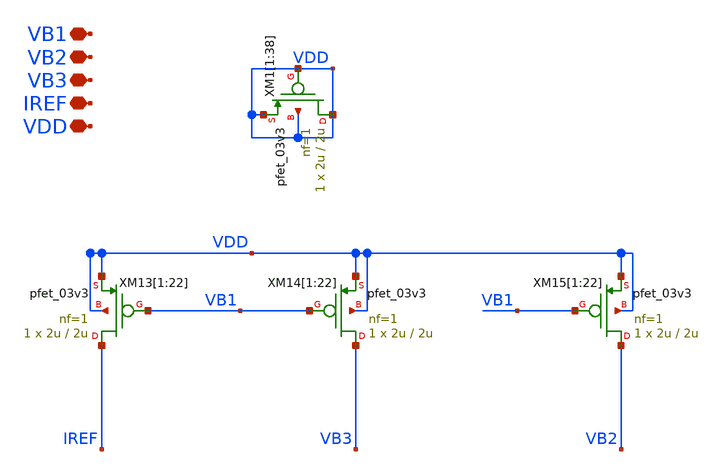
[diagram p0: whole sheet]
** sch_path: TIA_Filter/Folded/FC_bias_pfets.sch
**.subckt FC_bias_pfets IREF VDD VB1 VB2 VB3
*.iopin IREF
*.iopin VDD
*.iopin VB1
*.iopin VB2
*.iopin VB3
XM13[1] IREF VB1 VDD VDD pfet_03v3 L=2u W=2u nf=1 ad='int((nf+1)/2) * W/nf * 0.18u' as='int((nf+2)/2) * W/nf * 0.18u'
+ pd='2*int((nf+1)/2) * (W/nf + 0.18u)' ps='2*int((nf+2)/2) * (W/nf + 0.18u)' nrd='0.18u / W' nrs='0.18u / W'
+ sa=0 sb=0 sd=0 m=1
XM13[2] IREF VB1 VDD VDD pfet_03v3 L=2u W=2u nf=1 ad='int((nf+1)/2) * W/nf * 0.18u' as='int((nf+2)/2) * W/nf * 0.18u'
+ pd='2*int((nf+1)/2) * (W/nf + 0.18u)' ps='2*int((nf+2)/2) * (W/nf + 0.18u)' nrd='0.18u / W' nrs='0.18u / W'
+ sa=0 sb=0 sd=0 m=1
XM13[3] IREF VB1 VDD VDD pfet_03v3 L=2u W=2u nf=1 ad='int((nf+1)/2) * W/nf * 0.18u' as='int((nf+2)/2) * W/nf * 0.18u'
+ pd='2*int((nf+1)/2) * (W/nf + 0.18u)' ps='2*int((nf+2)/2) * (W/nf + 0.18u)' nrd='0.18u / W' nrs='0.18u / W'
+ sa=0 sb=0 sd=0 m=1
XM13[4] IREF VB1 VDD VDD pfet_03v3 L=2u W=2u nf=1 ad='int((nf+1)/2) * W/nf * 0.18u' as='int((nf+2)/2) * W/nf * 0.18u'
+ pd='2*int((nf+1)/2) * (W/nf + 0.18u)' ps='2*int((nf+2)/2) * (W/nf + 0.18u)' nrd='0.18u / W' nrs='0.18u / W'
+ sa=0 sb=0 sd=0 m=1
XM13[5] IREF VB1 VDD VDD pfet_03v3 L=2u W=2u nf=1 ad='int((nf+1)/2) * W/nf * 0.18u' as='int((nf+2)/2) * W/nf * 0.18u'
+ pd='2*int((nf+1)/2) * (W/nf + 0.18u)' ps='2*int((nf+2)/2) * (W/nf + 0.18u)' nrd='0.18u / W' nrs='0.18u / W'
+ sa=0 sb=0 sd=0 m=1
XM13[6] IREF VB1 VDD VDD pfet_03v3 L=2u W=2u nf=1 ad='int((nf+1)/2) * W/nf * 0.18u' as='int((nf+2)/2) * W/nf * 0.18u'
+ pd='2*int((nf+1)/2) * (W/nf + 0.18u)' ps='2*int((nf+2)/2) * (W/nf + 0.18u)' nrd='0.18u / W' nrs='0.18u / W'
+ sa=0 sb=0 sd=0 m=1
XM13[7] IREF VB1 VDD VDD pfet_03v3 L=2u W=2u nf=1 ad='int((nf+1)/2) * W/nf * 0.18u' as='int((nf+2)/2) * W/nf * 0.18u'
+ pd='2*int((nf+1)/2) * (W/nf + 0.18u)' ps='2*int((nf+2)/2) * (W/nf + 0.18u)' nrd='0.18u / W' nrs='0.18u / W'
+ sa=0 sb=0 sd=0 m=1
XM13[8] IREF VB1 VDD VDD pfet_03v3 L=2u W=2u nf=1 ad='int((nf+1)/2) * W/nf * 0.18u' as='int((nf+2)/2) * W/nf * 0.18u'
+ pd='2*int((nf+1)/2) * (W/nf + 0.18u)' ps='2*int((nf+2)/2) * (W/nf + 0.18u)' nrd='0.18u / W' nrs='0.18u / W'
+ sa=0 sb=0 sd=0 m=1
XM13[9] IREF VB1 VDD VDD pfet_03v3 L=2u W=2u nf=1 ad='int((nf+1)/2) * W/nf * 0.18u' as='int((nf+2)/2) * W/nf * 0.18u'
+ pd='2*int((nf+1)/2) * (W/nf + 0.18u)' ps='2*int((nf+2)/2) * (W/nf + 0.18u)' nrd='0.18u / W' nrs='0.18u / W'
+ sa=0 sb=0 sd=0 m=1
XM13[10] IREF VB1 VDD VDD pfet_03v3 L=2u W=2u nf=1 ad='int((nf+1)/2) * W/nf * 0.18u' as='int((nf+2)/2) * W/nf * 0.18u'
+ pd='2*int((nf+1)/2) * (W/nf + 0.18u)' ps='2*int((nf+2)/2) * (W/nf + 0.18u)' nrd='0.18u / W' nrs='0.18u / W'
+ sa=0 sb=0 sd=0 m=1
XM13[11] IREF VB1 VDD VDD pfet_03v3 L=2u W=2u nf=1 ad='int((nf+1)/2) * W/nf * 0.18u' as='int((nf+2)/2) * W/nf * 0.18u'
+ pd='2*int((nf+1)/2) * (W/nf + 0.18u)' ps='2*int((nf+2)/2) * (W/nf + 0.18u)' nrd='0.18u / W' nrs='0.18u / W'
+ sa=0 sb=0 sd=0 m=1
XM13[12] IREF VB1 VDD VDD pfet_03v3 L=2u W=2u nf=1 ad='int((nf+1)/2) * W/nf * 0.18u' as='int((nf+2)/2) * W/nf * 0.18u'
+ pd='2*int((nf+1)/2) * (W/nf + 0.18u)' ps='2*int((nf+2)/2) * (W/nf + 0.18u)' nrd='0.18u / W' nrs='0.18u / W'
+ sa=0 sb=0 sd=0 m=1
XM13[13] IREF VB1 VDD VDD pfet_03v3 L=2u W=2u nf=1 ad='int((nf+1)/2) * W/nf * 0.18u' as='int((nf+2)/2) * W/nf * 0.18u'
+ pd='2*int((nf+1)/2) * (W/nf + 0.18u)' ps='2*int((nf+2)/2) * (W/nf + 0.18u)' nrd='0.18u / W' nrs='0.18u / W'
+ sa=0 sb=0 sd=0 m=1
XM13[14] IREF VB1 VDD VDD pfet_03v3 L=2u W=2u nf=1 ad='int((nf+1)/2) * W/nf * 0.18u' as='int((nf+2)/2) * W/nf * 0.18u'
+ pd='2*int((nf+1)/2) * (W/nf + 0.18u)' ps='2*int((nf+2)/2) * (W/nf + 0.18u)' nrd='0.18u / W' nrs='0.18u / W'
+ sa=0 sb=0 sd=0 m=1
XM13[15] IREF VB1 VDD VDD pfet_03v3 L=2u W=2u nf=1 ad='int((nf+1)/2) * W/nf * 0.18u' as='int((nf+2)/2) * W/nf * 0.18u'
+ pd='2*int((nf+1)/2) * (W/nf + 0.18u)' ps='2*int((nf+2)/2) * (W/nf + 0.18u)' nrd='0.18u / W' nrs='0.18u / W'
+ sa=0 sb=0 sd=0 m=1
XM13[16] IREF VB1 VDD VDD pfet_03v3 L=2u W=2u nf=1 ad='int((nf+1)/2) * W/nf * 0.18u' as='int((nf+2)/2) * W/nf * 0.18u'
+ pd='2*int((nf+1)/2) * (W/nf + 0.18u)' ps='2*int((nf+2)/2) * (W/nf + 0.18u)' nrd='0.18u / W' nrs='0.18u / W'
+ sa=0 sb=0 sd=0 m=1
XM13[17] IREF VB1 VDD VDD pfet_03v3 L=2u W=2u nf=1 ad='int((nf+1)/2) * W/nf * 0.18u' as='int((nf+2)/2) * W/nf * 0.18u'
+ pd='2*int((nf+1)/2) * (W/nf + 0.18u)' ps='2*int((nf+2)/2) * (W/nf + 0.18u)' nrd='0.18u / W' nrs='0.18u / W'
+ sa=0 sb=0 sd=0 m=1
XM13[18] IREF VB1 VDD VDD pfet_03v3 L=2u W=2u nf=1 ad='int((nf+1)/2) * W/nf * 0.18u' as='int((nf+2)/2) * W/nf * 0.18u'
+ pd='2*int((nf+1)/2) * (W/nf + 0.18u)' ps='2*int((nf+2)/2) * (W/nf + 0.18u)' nrd='0.18u / W' nrs='0.18u / W'
+ sa=0 sb=0 sd=0 m=1
XM13[19] IREF VB1 VDD VDD pfet_03v3 L=2u W=2u nf=1 ad='int((nf+1)/2) * W/nf * 0.18u' as='int((nf+2)/2) * W/nf * 0.18u'
+ pd='2*int((nf+1)/2) * (W/nf + 0.18u)' ps='2*int((nf+2)/2) * (W/nf + 0.18u)' nrd='0.18u / W' nrs='0.18u / W'
+ sa=0 sb=0 sd=0 m=1
XM13[20] IREF VB1 VDD VDD pfet_03v3 L=2u W=2u nf=1 ad='int((nf+1)/2) * W/nf * 0.18u' as='int((nf+2)/2) * W/nf * 0.18u'
+ pd='2*int((nf+1)/2) * (W/nf + 0.18u)' ps='2*int((nf+2)/2) * (W/nf + 0.18u)' nrd='0.18u / W' nrs='0.18u / W'
+ sa=0 sb=0 sd=0 m=1
XM13[21] IREF VB1 VDD VDD pfet_03v3 L=2u W=2u nf=1 ad='int((nf+1)/2) * W/nf * 0.18u' as='int((nf+2)/2) * W/nf * 0.18u'
+ pd='2*int((nf+1)/2) * (W/nf + 0.18u)' ps='2*int((nf+2)/2) * (W/nf + 0.18u)' nrd='0.18u / W' nrs='0.18u / W'
+ sa=0 sb=0 sd=0 m=1
XM13[22] IREF VB1 VDD VDD pfet_03v3 L=2u W=2u nf=1 ad='int((nf+1)/2) * W/nf * 0.18u' as='int((nf+2)/2) * W/nf * 0.18u'
+ pd='2*int((nf+1)/2) * (W/nf + 0.18u)' ps='2*int((nf+2)/2) * (W/nf + 0.18u)' nrd='0.18u / W' nrs='0.18u / W'
+ sa=0 sb=0 sd=0 m=1
XM14[1] VB3 VB1 VDD VDD pfet_03v3 L=2u W=2u nf=1 ad='int((nf+1)/2) * W/nf * 0.18u' as='int((nf+2)/2) * W/nf * 0.18u'
+ pd='2*int((nf+1)/2) * (W/nf + 0.18u)' ps='2*int((nf+2)/2) * (W/nf + 0.18u)' nrd='0.18u / W' nrs='0.18u / W'
+ sa=0 sb=0 sd=0 m=1
XM14[2] VB3 VB1 VDD VDD pfet_03v3 L=2u W=2u nf=1 ad='int((nf+1)/2) * W/nf * 0.18u' as='int((nf+2)/2) * W/nf * 0.18u'
+ pd='2*int((nf+1)/2) * (W/nf + 0.18u)' ps='2*int((nf+2)/2) * (W/nf + 0.18u)' nrd='0.18u / W' nrs='0.18u / W'
+ sa=0 sb=0 sd=0 m=1
XM14[3] VB3 VB1 VDD VDD pfet_03v3 L=2u W=2u nf=1 ad='int((nf+1)/2) * W/nf * 0.18u' as='int((nf+2)/2) * W/nf * 0.18u'
+ pd='2*int((nf+1)/2) * (W/nf + 0.18u)' ps='2*int((nf+2)/2) * (W/nf + 0.18u)' nrd='0.18u / W' nrs='0.18u / W'
+ sa=0 sb=0 sd=0 m=1
XM14[4] VB3 VB1 VDD VDD pfet_03v3 L=2u W=2u nf=1 ad='int((nf+1)/2) * W/nf * 0.18u' as='int((nf+2)/2) * W/nf * 0.18u'
+ pd='2*int((nf+1)/2) * (W/nf + 0.18u)' ps='2*int((nf+2)/2) * (W/nf + 0.18u)' nrd='0.18u / W' nrs='0.18u / W'
+ sa=0 sb=0 sd=0 m=1
XM14[5] VB3 VB1 VDD VDD pfet_03v3 L=2u W=2u nf=1 ad='int((nf+1)/2) * W/nf * 0.18u' as='int((nf+2)/2) * W/nf * 0.18u'
+ pd='2*int((nf+1)/2) * (W/nf + 0.18u)' ps='2*int((nf+2)/2) * (W/nf + 0.18u)' nrd='0.18u / W' nrs='0.18u / W'
+ sa=0 sb=0 sd=0 m=1
XM14[6] VB3 VB1 VDD VDD pfet_03v3 L=2u W=2u nf=1 ad='int((nf+1)/2) * W/nf * 0.18u' as='int((nf+2)/2) * W/nf * 0.18u'
+ pd='2*int((nf+1)/2) * (W/nf + 0.18u)' ps='2*int((nf+2)/2) * (W/nf + 0.18u)' nrd='0.18u / W' nrs='0.18u / W'
+ sa=0 sb=0 sd=0 m=1
XM14[7] VB3 VB1 VDD VDD pfet_03v3 L=2u W=2u nf=1 ad='int((nf+1)/2) * W/nf * 0.18u' as='int((nf+2)/2) * W/nf * 0.18u'
+ pd='2*int((nf+1)/2) * (W/nf + 0.18u)' ps='2*int((nf+2)/2) * (W/nf + 0.18u)' nrd='0.18u / W' nrs='0.18u / W'
+ sa=0 sb=0 sd=0 m=1
XM14[8] VB3 VB1 VDD VDD pfet_03v3 L=2u W=2u nf=1 ad='int((nf+1)/2) * W/nf * 0.18u' as='int((nf+2)/2) * W/nf * 0.18u'
+ pd='2*int((nf+1)/2) * (W/nf + 0.18u)' ps='2*int((nf+2)/2) * (W/nf + 0.18u)' nrd='0.18u / W' nrs='0.18u / W'
+ sa=0 sb=0 sd=0 m=1
XM14[9] VB3 VB1 VDD VDD pfet_03v3 L=2u W=2u nf=1 ad='int((nf+1)/2) * W/nf * 0.18u' as='int((nf+2)/2) * W/nf * 0.18u'
+ pd='2*int((nf+1)/2) * (W/nf + 0.18u)' ps='2*int((nf+2)/2) * (W/nf + 0.18u)' nrd='0.18u / W' nrs='0.18u / W'
+ sa=0 sb=0 sd=0 m=1
XM14[10] VB3 VB1 VDD VDD pfet_03v3 L=2u W=2u nf=1 ad='int((nf+1)/2) * W/nf * 0.18u' as='int((nf+2)/2) * W/nf * 0.18u'
+ pd='2*int((nf+1)/2) * (W/nf + 0.18u)' ps='2*int((nf+2)/2) * (W/nf + 0.18u)' nrd='0.18u / W' nrs='0.18u / W'
+ sa=0 sb=0 sd=0 m=1
XM14[11] VB3 VB1 VDD VDD pfet_03v3 L=2u W=2u nf=1 ad='int((nf+1)/2) * W/nf * 0.18u' as='int((nf+2)/2) * W/nf * 0.18u'
+ pd='2*int((nf+1)/2) * (W/nf + 0.18u)' ps='2*int((nf+2)/2) * (W/nf + 0.18u)' nrd='0.18u / W' nrs='0.18u / W'
+ sa=0 sb=0 sd=0 m=1
XM14[12] VB3 VB1 VDD VDD pfet_03v3 L=2u W=2u nf=1 ad='int((nf+1)/2) * W/nf * 0.18u' as='int((nf+2)/2) * W/nf * 0.18u'
+ pd='2*int((nf+1)/2) * (W/nf + 0.18u)' ps='2*int((nf+2)/2) * (W/nf + 0.18u)' nrd='0.18u / W' nrs='0.18u / W'
+ sa=0 sb=0 sd=0 m=1
XM14[13] VB3 VB1 VDD VDD pfet_03v3 L=2u W=2u nf=1 ad='int((nf+1)/2) * W/nf * 0.18u' as='int((nf+2)/2) * W/nf * 0.18u'
+ pd='2*int((nf+1)/2) * (W/nf + 0.18u)' ps='2*int((nf+2)/2) * (W/nf + 0.18u)' nrd='0.18u / W' nrs='0.18u / W'
+ sa=0 sb=0 sd=0 m=1
XM14[14] VB3 VB1 VDD VDD pfet_03v3 L=2u W=2u nf=1 ad='int((nf+1)/2) * W/nf * 0.18u' as='int((nf+2)/2) * W/nf * 0.18u'
+ pd='2*int((nf+1)/2) * (W/nf + 0.18u)' ps='2*int((nf+2)/2) * (W/nf + 0.18u)' nrd='0.18u / W' nrs='0.18u / W'
+ sa=0 sb=0 sd=0 m=1
XM14[15] VB3 VB1 VDD VDD pfet_03v3 L=2u W=2u nf=1 ad='int((nf+1)/2) * W/nf * 0.18u' as='int((nf+2)/2) * W/nf * 0.18u'
+ pd='2*int((nf+1)/2) * (W/nf + 0.18u)' ps='2*int((nf+2)/2) * (W/nf + 0.18u)' nrd='0.18u / W' nrs='0.18u / W'
+ sa=0 sb=0 sd=0 m=1
XM14[16] VB3 VB1 VDD VDD pfet_03v3 L=2u W=2u nf=1 ad='int((nf+1)/2) * W/nf * 0.18u' as='int((nf+2)/2) * W/nf * 0.18u'
+ pd='2*int((nf+1)/2) * (W/nf + 0.18u)' ps='2*int((nf+2)/2) * (W/nf + 0.18u)' nrd='0.18u / W' nrs='0.18u / W'
+ sa=0 sb=0 sd=0 m=1
XM14[17] VB3 VB1 VDD VDD pfet_03v3 L=2u W=2u nf=1 ad='int((nf+1)/2) * W/nf * 0.18u' as='int((nf+2)/2) * W/nf * 0.18u'
+ pd='2*int((nf+1)/2) * (W/nf + 0.18u)' ps='2*int((nf+2)/2) * (W/nf + 0.18u)' nrd='0.18u / W' nrs='0.18u / W'
+ sa=0 sb=0 sd=0 m=1
XM14[18] VB3 VB1 VDD VDD pfet_03v3 L=2u W=2u nf=1 ad='int((nf+1)/2) * W/nf * 0.18u' as='int((nf+2)/2) * W/nf * 0.18u'
+ pd='2*int((nf+1)/2) * (W/nf + 0.18u)' ps='2*int((nf+2)/2) * (W/nf + 0.18u)' nrd='0.18u / W' nrs='0.18u / W'
+ sa=0 sb=0 sd=0 m=1
XM14[19] VB3 VB1 VDD VDD pfet_03v3 L=2u W=2u nf=1 ad='int((nf+1)/2) * W/nf * 0.18u' as='int((nf+2)/2) * W/nf * 0.18u'
+ pd='2*int((nf+1)/2) * (W/nf + 0.18u)' ps='2*int((nf+2)/2) * (W/nf + 0.18u)' nrd='0.18u / W' nrs='0.18u / W'
+ sa=0 sb=0 sd=0 m=1
XM14[20] VB3 VB1 VDD VDD pfet_03v3 L=2u W=2u nf=1 ad='int((nf+1)/2) * W/nf * 0.18u' as='int((nf+2)/2) * W/nf * 0.18u'
+ pd='2*int((nf+1)/2) * (W/nf + 0.18u)' ps='2*int((nf+2)/2) * (W/nf + 0.18u)' nrd='0.18u / W' nrs='0.18u / W'
+ sa=0 sb=0 sd=0 m=1
XM14[21] VB3 VB1 VDD VDD pfet_03v3 L=2u W=2u nf=1 ad='int((nf+1)/2) * W/nf * 0.18u' as='int((nf+2)/2) * W/nf * 0.18u'
+ pd='2*int((nf+1)/2) * (W/nf + 0.18u)' ps='2*int((nf+2)/2) * (W/nf + 0.18u)' nrd='0.18u / W' nrs='0.18u / W'
+ sa=0 sb=0 sd=0 m=1
XM14[22] VB3 VB1 VDD VDD pfet_03v3 L=2u W=2u nf=1 ad='int((nf+1)/2) * W/nf * 0.18u' as='int((nf+2)/2) * W/nf * 0.18u'
+ pd='2*int((nf+1)/2) * (W/nf + 0.18u)' ps='2*int((nf+2)/2) * (W/nf + 0.18u)' nrd='0.18u / W' nrs='0.18u / W'
+ sa=0 sb=0 sd=0 m=1
XM15[1] VB2 VB1 VDD VDD pfet_03v3 L=2u W=2u nf=1 ad='int((nf+1)/2) * W/nf * 0.18u' as='int((nf+2)/2) * W/nf * 0.18u'
+ pd='2*int((nf+1)/2) * (W/nf + 0.18u)' ps='2*int((nf+2)/2) * (W/nf + 0.18u)' nrd='0.18u / W' nrs='0.18u / W'
+ sa=0 sb=0 sd=0 m=1
XM15[2] VB2 VB1 VDD VDD pfet_03v3 L=2u W=2u nf=1 ad='int((nf+1)/2) * W/nf * 0.18u' as='int((nf+2)/2) * W/nf * 0.18u'
+ pd='2*int((nf+1)/2) * (W/nf + 0.18u)' ps='2*int((nf+2)/2) * (W/nf + 0.18u)' nrd='0.18u / W' nrs='0.18u / W'
+ sa=0 sb=0 sd=0 m=1
XM15[3] VB2 VB1 VDD VDD pfet_03v3 L=2u W=2u nf=1 ad='int((nf+1)/2) * W/nf * 0.18u' as='int((nf+2)/2) * W/nf * 0.18u'
+ pd='2*int((nf+1)/2) * (W/nf + 0.18u)' ps='2*int((nf+2)/2) * (W/nf + 0.18u)' nrd='0.18u / W' nrs='0.18u / W'
+ sa=0 sb=0 sd=0 m=1
XM15[4] VB2 VB1 VDD VDD pfet_03v3 L=2u W=2u nf=1 ad='int((nf+1)/2) * W/nf * 0.18u' as='int((nf+2)/2) * W/nf * 0.18u'
+ pd='2*int((nf+1)/2) * (W/nf + 0.18u)' ps='2*int((nf+2)/2) * (W/nf + 0.18u)' nrd='0.18u / W' nrs='0.18u / W'
+ sa=0 sb=0 sd=0 m=1
XM15[5] VB2 VB1 VDD VDD pfet_03v3 L=2u W=2u nf=1 ad='int((nf+1)/2) * W/nf * 0.18u' as='int((nf+2)/2) * W/nf * 0.18u'
+ pd='2*int((nf+1)/2) * (W/nf + 0.18u)' ps='2*int((nf+2)/2) * (W/nf + 0.18u)' nrd='0.18u / W' nrs='0.18u / W'
+ sa=0 sb=0 sd=0 m=1
XM15[6] VB2 VB1 VDD VDD pfet_03v3 L=2u W=2u nf=1 ad='int((nf+1)/2) * W/nf * 0.18u' as='int((nf+2)/2) * W/nf * 0.18u'
+ pd='2*int((nf+1)/2) * (W/nf + 0.18u)' ps='2*int((nf+2)/2) * (W/nf + 0.18u)' nrd='0.18u / W' nrs='0.18u / W'
+ sa=0 sb=0 sd=0 m=1
XM15[7] VB2 VB1 VDD VDD pfet_03v3 L=2u W=2u nf=1 ad='int((nf+1)/2) * W/nf * 0.18u' as='int((nf+2)/2) * W/nf * 0.18u'
+ pd='2*int((nf+1)/2) * (W/nf + 0.18u)' ps='2*int((nf+2)/2) * (W/nf + 0.18u)' nrd='0.18u / W' nrs='0.18u / W'
+ sa=0 sb=0 sd=0 m=1
XM15[8] VB2 VB1 VDD VDD pfet_03v3 L=2u W=2u nf=1 ad='int((nf+1)/2) * W/nf * 0.18u' as='int((nf+2)/2) * W/nf * 0.18u'
+ pd='2*int((nf+1)/2) * (W/nf + 0.18u)' ps='2*int((nf+2)/2) * (W/nf + 0.18u)' nrd='0.18u / W' nrs='0.18u / W'
+ sa=0 sb=0 sd=0 m=1
XM15[9] VB2 VB1 VDD VDD pfet_03v3 L=2u W=2u nf=1 ad='int((nf+1)/2) * W/nf * 0.18u' as='int((nf+2)/2) * W/nf * 0.18u'
+ pd='2*int((nf+1)/2) * (W/nf + 0.18u)' ps='2*int((nf+2)/2) * (W/nf + 0.18u)' nrd='0.18u / W' nrs='0.18u / W'
+ sa=0 sb=0 sd=0 m=1
XM15[10] VB2 VB1 VDD VDD pfet_03v3 L=2u W=2u nf=1 ad='int((nf+1)/2) * W/nf * 0.18u' as='int((nf+2)/2) * W/nf * 0.18u'
+ pd='2*int((nf+1)/2) * (W/nf + 0.18u)' ps='2*int((nf+2)/2) * (W/nf + 0.18u)' nrd='0.18u / W' nrs='0.18u / W'
+ sa=0 sb=0 sd=0 m=1
XM15[11] VB2 VB1 VDD VDD pfet_03v3 L=2u W=2u nf=1 ad='int((nf+1)/2) * W/nf * 0.18u' as='int((nf+2)/2) * W/nf * 0.18u'
+ pd='2*int((nf+1)/2) * (W/nf + 0.18u)' ps='2*int((nf+2)/2) * (W/nf + 0.18u)' nrd='0.18u / W' nrs='0.18u / W'
+ sa=0 sb=0 sd=0 m=1
XM15[12] VB2 VB1 VDD VDD pfet_03v3 L=2u W=2u nf=1 ad='int((nf+1)/2) * W/nf * 0.18u' as='int((nf+2)/2) * W/nf * 0.18u'
+ pd='2*int((nf+1)/2) * (W/nf + 0.18u)' ps='2*int((nf+2)/2) * (W/nf + 0.18u)' nrd='0.18u / W' nrs='0.18u / W'
+ sa=0 sb=0 sd=0 m=1
XM15[13] VB2 VB1 VDD VDD pfet_03v3 L=2u W=2u nf=1 ad='int((nf+1)/2) * W/nf * 0.18u' as='int((nf+2)/2) * W/nf * 0.18u'
+ pd='2*int((nf+1)/2) * (W/nf + 0.18u)' ps='2*int((nf+2)/2) * (W/nf + 0.18u)' nrd='0.18u / W' nrs='0.18u / W'
+ sa=0 sb=0 sd=0 m=1
XM15[14] VB2 VB1 VDD VDD pfet_03v3 L=2u W=2u nf=1 ad='int((nf+1)/2) * W/nf * 0.18u' as='int((nf+2)/2) * W/nf * 0.18u'
+ pd='2*int((nf+1)/2) * (W/nf + 0.18u)' ps='2*int((nf+2)/2) * (W/nf + 0.18u)' nrd='0.18u / W' nrs='0.18u / W'
+ sa=0 sb=0 sd=0 m=1
XM15[15] VB2 VB1 VDD VDD pfet_03v3 L=2u W=2u nf=1 ad='int((nf+1)/2) * W/nf * 0.18u' as='int((nf+2)/2) * W/nf * 0.18u'
+ pd='2*int((nf+1)/2) * (W/nf + 0.18u)' ps='2*int((nf+2)/2) * (W/nf + 0.18u)' nrd='0.18u / W' nrs='0.18u / W'
+ sa=0 sb=0 sd=0 m=1
XM15[16] VB2 VB1 VDD VDD pfet_03v3 L=2u W=2u nf=1 ad='int((nf+1)/2) * W/nf * 0.18u' as='int((nf+2)/2) * W/nf * 0.18u'
+ pd='2*int((nf+1)/2) * (W/nf + 0.18u)' ps='2*int((nf+2)/2) * (W/nf + 0.18u)' nrd='0.18u / W' nrs='0.18u / W'
+ sa=0 sb=0 sd=0 m=1
XM15[17] VB2 VB1 VDD VDD pfet_03v3 L=2u W=2u nf=1 ad='int((nf+1)/2) * W/nf * 0.18u' as='int((nf+2)/2) * W/nf * 0.18u'
+ pd='2*int((nf+1)/2) * (W/nf + 0.18u)' ps='2*int((nf+2)/2) * (W/nf + 0.18u)' nrd='0.18u / W' nrs='0.18u / W'
+ sa=0 sb=0 sd=0 m=1
XM15[18] VB2 VB1 VDD VDD pfet_03v3 L=2u W=2u nf=1 ad='int((nf+1)/2) * W/nf * 0.18u' as='int((nf+2)/2) * W/nf * 0.18u'
+ pd='2*int((nf+1)/2) * (W/nf + 0.18u)' ps='2*int((nf+2)/2) * (W/nf + 0.18u)' nrd='0.18u / W' nrs='0.18u / W'
+ sa=0 sb=0 sd=0 m=1
XM15[19] VB2 VB1 VDD VDD pfet_03v3 L=2u W=2u nf=1 ad='int((nf+1)/2) * W/nf * 0.18u' as='int((nf+2)/2) * W/nf * 0.18u'
+ pd='2*int((nf+1)/2) * (W/nf + 0.18u)' ps='2*int((nf+2)/2) * (W/nf + 0.18u)' nrd='0.18u / W' nrs='0.18u / W'
+ sa=0 sb=0 sd=0 m=1
XM15[20] VB2 VB1 VDD VDD pfet_03v3 L=2u W=2u nf=1 ad='int((nf+1)/2) * W/nf * 0.18u' as='int((nf+2)/2) * W/nf * 0.18u'
+ pd='2*int((nf+1)/2) * (W/nf + 0.18u)' ps='2*int((nf+2)/2) * (W/nf + 0.18u)' nrd='0.18u / W' nrs='0.18u / W'
+ sa=0 sb=0 sd=0 m=1
XM15[21] VB2 VB1 VDD VDD pfet_03v3 L=2u W=2u nf=1 ad='int((nf+1)/2) * W/nf * 0.18u' as='int((nf+2)/2) * W/nf * 0.18u'
+ pd='2*int((nf+1)/2) * (W/nf + 0.18u)' ps='2*int((nf+2)/2) * (W/nf + 0.18u)' nrd='0.18u / W' nrs='0.18u / W'
+ sa=0 sb=0 sd=0 m=1
XM15[22] VB2 VB1 VDD VDD pfet_03v3 L=2u W=2u nf=1 ad='int((nf+1)/2) * W/nf * 0.18u' as='int((nf+2)/2) * W/nf * 0.18u'
+ pd='2*int((nf+1)/2) * (W/nf + 0.18u)' ps='2*int((nf+2)/2) * (W/nf + 0.18u)' nrd='0.18u / W' nrs='0.18u / W'
+ sa=0 sb=0 sd=0 m=1
XM1[1] VDD VDD VDD VDD pfet_03v3 L=2u W=2u nf=1 ad='int((nf+1)/2) * W/nf * 0.18u' as='int((nf+2)/2) * W/nf * 0.18u'
+ pd='2*int((nf+1)/2) * (W/nf + 0.18u)' ps='2*int((nf+2)/2) * (W/nf + 0.18u)' nrd='0.18u / W' nrs='0.18u / W'
+ sa=0 sb=0 sd=0 m=1
XM1[2] VDD VDD VDD VDD pfet_03v3 L=2u W=2u nf=1 ad='int((nf+1)/2) * W/nf * 0.18u' as='int((nf+2)/2) * W/nf * 0.18u'
+ pd='2*int((nf+1)/2) * (W/nf + 0.18u)' ps='2*int((nf+2)/2) * (W/nf + 0.18u)' nrd='0.18u / W' nrs='0.18u / W'
+ sa=0 sb=0 sd=0 m=1
XM1[3] VDD VDD VDD VDD pfet_03v3 L=2u W=2u nf=1 ad='int((nf+1)/2) * W/nf * 0.18u' as='int((nf+2)/2) * W/nf * 0.18u'
+ pd='2*int((nf+1)/2) * (W/nf + 0.18u)' ps='2*int((nf+2)/2) * (W/nf + 0.18u)' nrd='0.18u / W' nrs='0.18u / W'
+ sa=0 sb=0 sd=0 m=1
XM1[4] VDD VDD VDD VDD pfet_03v3 L=2u W=2u nf=1 ad='int((nf+1)/2) * W/nf * 0.18u' as='int((nf+2)/2) * W/nf * 0.18u'
+ pd='2*int((nf+1)/2) * (W/nf + 0.18u)' ps='2*int((nf+2)/2) * (W/nf + 0.18u)' nrd='0.18u / W' nrs='0.18u / W'
+ sa=0 sb=0 sd=0 m=1
XM1[5] VDD VDD VDD VDD pfet_03v3 L=2u W=2u nf=1 ad='int((nf+1)/2) * W/nf * 0.18u' as='int((nf+2)/2) * W/nf * 0.18u'
+ pd='2*int((nf+1)/2) * (W/nf + 0.18u)' ps='2*int((nf+2)/2) * (W/nf + 0.18u)' nrd='0.18u / W' nrs='0.18u / W'
+ sa=0 sb=0 sd=0 m=1
XM1[6] VDD VDD VDD VDD pfet_03v3 L=2u W=2u nf=1 ad='int((nf+1)/2) * W/nf * 0.18u' as='int((nf+2)/2) * W/nf * 0.18u'
+ pd='2*int((nf+1)/2) * (W/nf + 0.18u)' ps='2*int((nf+2)/2) * (W/nf + 0.18u)' nrd='0.18u / W' nrs='0.18u / W'
+ sa=0 sb=0 sd=0 m=1
XM1[7] VDD VDD VDD VDD pfet_03v3 L=2u W=2u nf=1 ad='int((nf+1)/2) * W/nf * 0.18u' as='int((nf+2)/2) * W/nf * 0.18u'
+ pd='2*int((nf+1)/2) * (W/nf + 0.18u)' ps='2*int((nf+2)/2) * (W/nf + 0.18u)' nrd='0.18u / W' nrs='0.18u / W'
+ sa=0 sb=0 sd=0 m=1
XM1[8] VDD VDD VDD VDD pfet_03v3 L=2u W=2u nf=1 ad='int((nf+1)/2) * W/nf * 0.18u' as='int((nf+2)/2) * W/nf * 0.18u'
+ pd='2*int((nf+1)/2) * (W/nf + 0.18u)' ps='2*int((nf+2)/2) * (W/nf + 0.18u)' nrd='0.18u / W' nrs='0.18u / W'
+ sa=0 sb=0 sd=0 m=1
XM1[9] VDD VDD VDD VDD pfet_03v3 L=2u W=2u nf=1 ad='int((nf+1)/2) * W/nf * 0.18u' as='int((nf+2)/2) * W/nf * 0.18u'
+ pd='2*int((nf+1)/2) * (W/nf + 0.18u)' ps='2*int((nf+2)/2) * (W/nf + 0.18u)' nrd='0.18u / W' nrs='0.18u / W'
+ sa=0 sb=0 sd=0 m=1
XM1[10] VDD VDD VDD VDD pfet_03v3 L=2u W=2u nf=1 ad='int((nf+1)/2) * W/nf * 0.18u' as='int((nf+2)/2) * W/nf * 0.18u'
+ pd='2*int((nf+1)/2) * (W/nf + 0.18u)' ps='2*int((nf+2)/2) * (W/nf + 0.18u)' nrd='0.18u / W' nrs='0.18u / W'
+ sa=0 sb=0 sd=0 m=1
XM1[11] VDD VDD VDD VDD pfet_03v3 L=2u W=2u nf=1 ad='int((nf+1)/2) * W/nf * 0.18u' as='int((nf+2)/2) * W/nf * 0.18u'
+ pd='2*int((nf+1)/2) * (W/nf + 0.18u)' ps='2*int((nf+2)/2) * (W/nf + 0.18u)' nrd='0.18u / W' nrs='0.18u / W'
+ sa=0 sb=0 sd=0 m=1
XM1[12] VDD VDD VDD VDD pfet_03v3 L=2u W=2u nf=1 ad='int((nf+1)/2) * W/nf * 0.18u' as='int((nf+2)/2) * W/nf * 0.18u'
+ pd='2*int((nf+1)/2) * (W/nf + 0.18u)' ps='2*int((nf+2)/2) * (W/nf + 0.18u)' nrd='0.18u / W' nrs='0.18u / W'
+ sa=0 sb=0 sd=0 m=1
XM1[13] VDD VDD VDD VDD pfet_03v3 L=2u W=2u nf=1 ad='int((nf+1)/2) * W/nf * 0.18u' as='int((nf+2)/2) * W/nf * 0.18u'
+ pd='2*int((nf+1)/2) * (W/nf + 0.18u)' ps='2*int((nf+2)/2) * (W/nf + 0.18u)' nrd='0.18u / W' nrs='0.18u / W'
+ sa=0 sb=0 sd=0 m=1
XM1[14] VDD VDD VDD VDD pfet_03v3 L=2u W=2u nf=1 ad='int((nf+1)/2) * W/nf * 0.18u' as='int((nf+2)/2) * W/nf * 0.18u'
+ pd='2*int((nf+1)/2) * (W/nf + 0.18u)' ps='2*int((nf+2)/2) * (W/nf + 0.18u)' nrd='0.18u / W' nrs='0.18u / W'
+ sa=0 sb=0 sd=0 m=1
XM1[15] VDD VDD VDD VDD pfet_03v3 L=2u W=2u nf=1 ad='int((nf+1)/2) * W/nf * 0.18u' as='int((nf+2)/2) * W/nf * 0.18u'
+ pd='2*int((nf+1)/2) * (W/nf + 0.18u)' ps='2*int((nf+2)/2) * (W/nf + 0.18u)' nrd='0.18u / W' nrs='0.18u / W'
+ sa=0 sb=0 sd=0 m=1
XM1[16] VDD VDD VDD VDD pfet_03v3 L=2u W=2u nf=1 ad='int((nf+1)/2) * W/nf * 0.18u' as='int((nf+2)/2) * W/nf * 0.18u'
+ pd='2*int((nf+1)/2) * (W/nf + 0.18u)' ps='2*int((nf+2)/2) * (W/nf + 0.18u)' nrd='0.18u / W' nrs='0.18u / W'
+ sa=0 sb=0 sd=0 m=1
XM1[17] VDD VDD VDD VDD pfet_03v3 L=2u W=2u nf=1 ad='int((nf+1)/2) * W/nf * 0.18u' as='int((nf+2)/2) * W/nf * 0.18u'
+ pd='2*int((nf+1)/2) * (W/nf + 0.18u)' ps='2*int((nf+2)/2) * (W/nf + 0.18u)' nrd='0.18u / W' nrs='0.18u / W'
+ sa=0 sb=0 sd=0 m=1
XM1[18] VDD VDD VDD VDD pfet_03v3 L=2u W=2u nf=1 ad='int((nf+1)/2) * W/nf * 0.18u' as='int((nf+2)/2) * W/nf * 0.18u'
+ pd='2*int((nf+1)/2) * (W/nf + 0.18u)' ps='2*int((nf+2)/2) * (W/nf + 0.18u)' nrd='0.18u / W' nrs='0.18u / W'
+ sa=0 sb=0 sd=0 m=1
XM1[19] VDD VDD VDD VDD pfet_03v3 L=2u W=2u nf=1 ad='int((nf+1)/2) * W/nf * 0.18u' as='int((nf+2)/2) * W/nf * 0.18u'
+ pd='2*int((nf+1)/2) * (W/nf + 0.18u)' ps='2*int((nf+2)/2) * (W/nf + 0.18u)' nrd='0.18u / W' nrs='0.18u / W'
+ sa=0 sb=0 sd=0 m=1
XM1[20] VDD VDD VDD VDD pfet_03v3 L=2u W=2u nf=1 ad='int((nf+1)/2) * W/nf * 0.18u' as='int((nf+2)/2) * W/nf * 0.18u'
+ pd='2*int((nf+1)/2) * (W/nf + 0.18u)' ps='2*int((nf+2)/2) * (W/nf + 0.18u)' nrd='0.18u / W' nrs='0.18u / W'
+ sa=0 sb=0 sd=0 m=1
XM1[21] VDD VDD VDD VDD pfet_03v3 L=2u W=2u nf=1 ad='int((nf+1)/2) * W/nf * 0.18u' as='int((nf+2)/2) * W/nf * 0.18u'
+ pd='2*int((nf+1)/2) * (W/nf + 0.18u)' ps='2*int((nf+2)/2) * (W/nf + 0.18u)' nrd='0.18u / W' nrs='0.18u / W'
+ sa=0 sb=0 sd=0 m=1
XM1[22] VDD VDD VDD VDD pfet_03v3 L=2u W=2u nf=1 ad='int((nf+1)/2) * W/nf * 0.18u' as='int((nf+2)/2) * W/nf * 0.18u'
+ pd='2*int((nf+1)/2) * (W/nf + 0.18u)' ps='2*int((nf+2)/2) * (W/nf + 0.18u)' nrd='0.18u / W' nrs='0.18u / W'
+ sa=0 sb=0 sd=0 m=1
XM1[23] VDD VDD VDD VDD pfet_03v3 L=2u W=2u nf=1 ad='int((nf+1)/2) * W/nf * 0.18u' as='int((nf+2)/2) * W/nf * 0.18u'
+ pd='2*int((nf+1)/2) * (W/nf + 0.18u)' ps='2*int((nf+2)/2) * (W/nf + 0.18u)' nrd='0.18u / W' nrs='0.18u / W'
+ sa=0 sb=0 sd=0 m=1
XM1[24] VDD VDD VDD VDD pfet_03v3 L=2u W=2u nf=1 ad='int((nf+1)/2) * W/nf * 0.18u' as='int((nf+2)/2) * W/nf * 0.18u'
+ pd='2*int((nf+1)/2) * (W/nf + 0.18u)' ps='2*int((nf+2)/2) * (W/nf + 0.18u)' nrd='0.18u / W' nrs='0.18u / W'
+ sa=0 sb=0 sd=0 m=1
XM1[25] VDD VDD VDD VDD pfet_03v3 L=2u W=2u nf=1 ad='int((nf+1)/2) * W/nf * 0.18u' as='int((nf+2)/2) * W/nf * 0.18u'
+ pd='2*int((nf+1)/2) * (W/nf + 0.18u)' ps='2*int((nf+2)/2) * (W/nf + 0.18u)' nrd='0.18u / W' nrs='0.18u / W'
+ sa=0 sb=0 sd=0 m=1
XM1[26] VDD VDD VDD VDD pfet_03v3 L=2u W=2u nf=1 ad='int((nf+1)/2) * W/nf * 0.18u' as='int((nf+2)/2) * W/nf * 0.18u'
+ pd='2*int((nf+1)/2) * (W/nf + 0.18u)' ps='2*int((nf+2)/2) * (W/nf + 0.18u)' nrd='0.18u / W' nrs='0.18u / W'
+ sa=0 sb=0 sd=0 m=1
XM1[27] VDD VDD VDD VDD pfet_03v3 L=2u W=2u nf=1 ad='int((nf+1)/2) * W/nf * 0.18u' as='int((nf+2)/2) * W/nf * 0.18u'
+ pd='2*int((nf+1)/2) * (W/nf + 0.18u)' ps='2*int((nf+2)/2) * (W/nf + 0.18u)' nrd='0.18u / W' nrs='0.18u / W'
+ sa=0 sb=0 sd=0 m=1
XM1[28] VDD VDD VDD VDD pfet_03v3 L=2u W=2u nf=1 ad='int((nf+1)/2) * W/nf * 0.18u' as='int((nf+2)/2) * W/nf * 0.18u'
+ pd='2*int((nf+1)/2) * (W/nf + 0.18u)' ps='2*int((nf+2)/2) * (W/nf + 0.18u)' nrd='0.18u / W' nrs='0.18u / W'
+ sa=0 sb=0 sd=0 m=1
XM1[29] VDD VDD VDD VDD pfet_03v3 L=2u W=2u nf=1 ad='int((nf+1)/2) * W/nf * 0.18u' as='int((nf+2)/2) * W/nf * 0.18u'
+ pd='2*int((nf+1)/2) * (W/nf + 0.18u)' ps='2*int((nf+2)/2) * (W/nf + 0.18u)' nrd='0.18u / W' nrs='0.18u / W'
+ sa=0 sb=0 sd=0 m=1
XM1[30] VDD VDD VDD VDD pfet_03v3 L=2u W=2u nf=1 ad='int((nf+1)/2) * W/nf * 0.18u' as='int((nf+2)/2) * W/nf * 0.18u'
+ pd='2*int((nf+1)/2) * (W/nf + 0.18u)' ps='2*int((nf+2)/2) * (W/nf + 0.18u)' nrd='0.18u / W' nrs='0.18u / W'
+ sa=0 sb=0 sd=0 m=1
XM1[31] VDD VDD VDD VDD pfet_03v3 L=2u W=2u nf=1 ad='int((nf+1)/2) * W/nf * 0.18u' as='int((nf+2)/2) * W/nf * 0.18u'
+ pd='2*int((nf+1)/2) * (W/nf + 0.18u)' ps='2*int((nf+2)/2) * (W/nf + 0.18u)' nrd='0.18u / W' nrs='0.18u / W'
+ sa=0 sb=0 sd=0 m=1
XM1[32] VDD VDD VDD VDD pfet_03v3 L=2u W=2u nf=1 ad='int((nf+1)/2) * W/nf * 0.18u' as='int((nf+2)/2) * W/nf * 0.18u'
+ pd='2*int((nf+1)/2) * (W/nf + 0.18u)' ps='2*int((nf+2)/2) * (W/nf + 0.18u)' nrd='0.18u / W' nrs='0.18u / W'
+ sa=0 sb=0 sd=0 m=1
XM1[33] VDD VDD VDD VDD pfet_03v3 L=2u W=2u nf=1 ad='int((nf+1)/2) * W/nf * 0.18u' as='int((nf+2)/2) * W/nf * 0.18u'
+ pd='2*int((nf+1)/2) * (W/nf + 0.18u)' ps='2*int((nf+2)/2) * (W/nf + 0.18u)' nrd='0.18u / W' nrs='0.18u / W'
+ sa=0 sb=0 sd=0 m=1
XM1[34] VDD VDD VDD VDD pfet_03v3 L=2u W=2u nf=1 ad='int((nf+1)/2) * W/nf * 0.18u' as='int((nf+2)/2) * W/nf * 0.18u'
+ pd='2*int((nf+1)/2) * (W/nf + 0.18u)' ps='2*int((nf+2)/2) * (W/nf + 0.18u)' nrd='0.18u / W' nrs='0.18u / W'
+ sa=0 sb=0 sd=0 m=1
XM1[35] VDD VDD VDD VDD pfet_03v3 L=2u W=2u nf=1 ad='int((nf+1)/2) * W/nf * 0.18u' as='int((nf+2)/2) * W/nf * 0.18u'
+ pd='2*int((nf+1)/2) * (W/nf + 0.18u)' ps='2*int((nf+2)/2) * (W/nf + 0.18u)' nrd='0.18u / W' nrs='0.18u / W'
+ sa=0 sb=0 sd=0 m=1
XM1[36] VDD VDD VDD VDD pfet_03v3 L=2u W=2u nf=1 ad='int((nf+1)/2) * W/nf * 0.18u' as='int((nf+2)/2) * W/nf * 0.18u'
+ pd='2*int((nf+1)/2) * (W/nf + 0.18u)' ps='2*int((nf+2)/2) * (W/nf + 0.18u)' nrd='0.18u / W' nrs='0.18u / W'
+ sa=0 sb=0 sd=0 m=1
XM1[37] VDD VDD VDD VDD pfet_03v3 L=2u W=2u nf=1 ad='int((nf+1)/2) * W/nf * 0.18u' as='int((nf+2)/2) * W/nf * 0.18u'
+ pd='2*int((nf+1)/2) * (W/nf + 0.18u)' ps='2*int((nf+2)/2) * (W/nf + 0.18u)' nrd='0.18u / W' nrs='0.18u / W'
+ sa=0 sb=0 sd=0 m=1
XM1[38] VDD VDD VDD VDD pfet_03v3 L=2u W=2u nf=1 ad='int((nf+1)/2) * W/nf * 0.18u' as='int((nf+2)/2) * W/nf * 0.18u'
+ pd='2*int((nf+1)/2) * (W/nf + 0.18u)' ps='2*int((nf+2)/2) * (W/nf + 0.18u)' nrd='0.18u / W' nrs='0.18u / W'
+ sa=0 sb=0 sd=0 m=1
**.ends
.end
